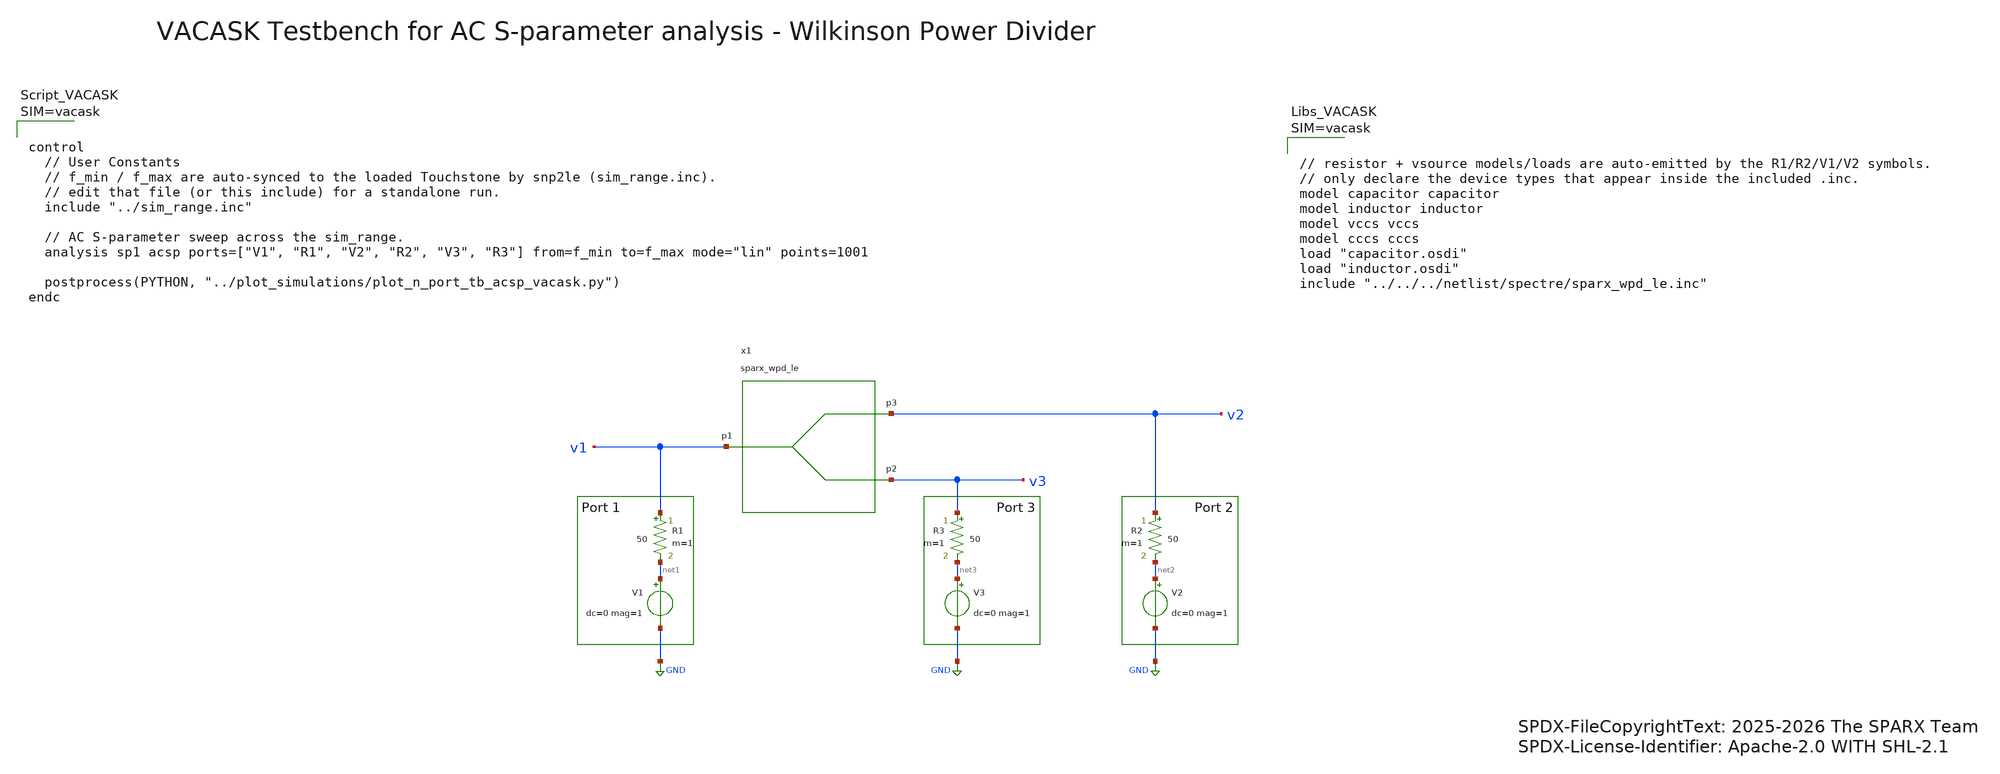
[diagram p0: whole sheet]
** sch_path: testbenches/xschem/sparx_wpd_le_tb_acsp_vacask.sch
* SPDX-FileCopyrightText: 2025-2026 The SPARX Team
* SPDX-License-Identifier: Apache-2.0 WITH SHL-2.1
**.subckt sparx_wpd_le_tb_acsp_vacask
R1 v1 net1 50 m=1
V1 net1 GND dc=0 mag=1
R2 v2 net2 50 m=1
V2 net2 GND dc=0 mag=1
R3 v3 net3 50 m=1
V3 net3 GND dc=0 mag=1
x1 v1 v3 v2 sparx_wpd_le
**** begin user architecture code






**** end user architecture code
**.ends
.GLOBAL GND
.end
